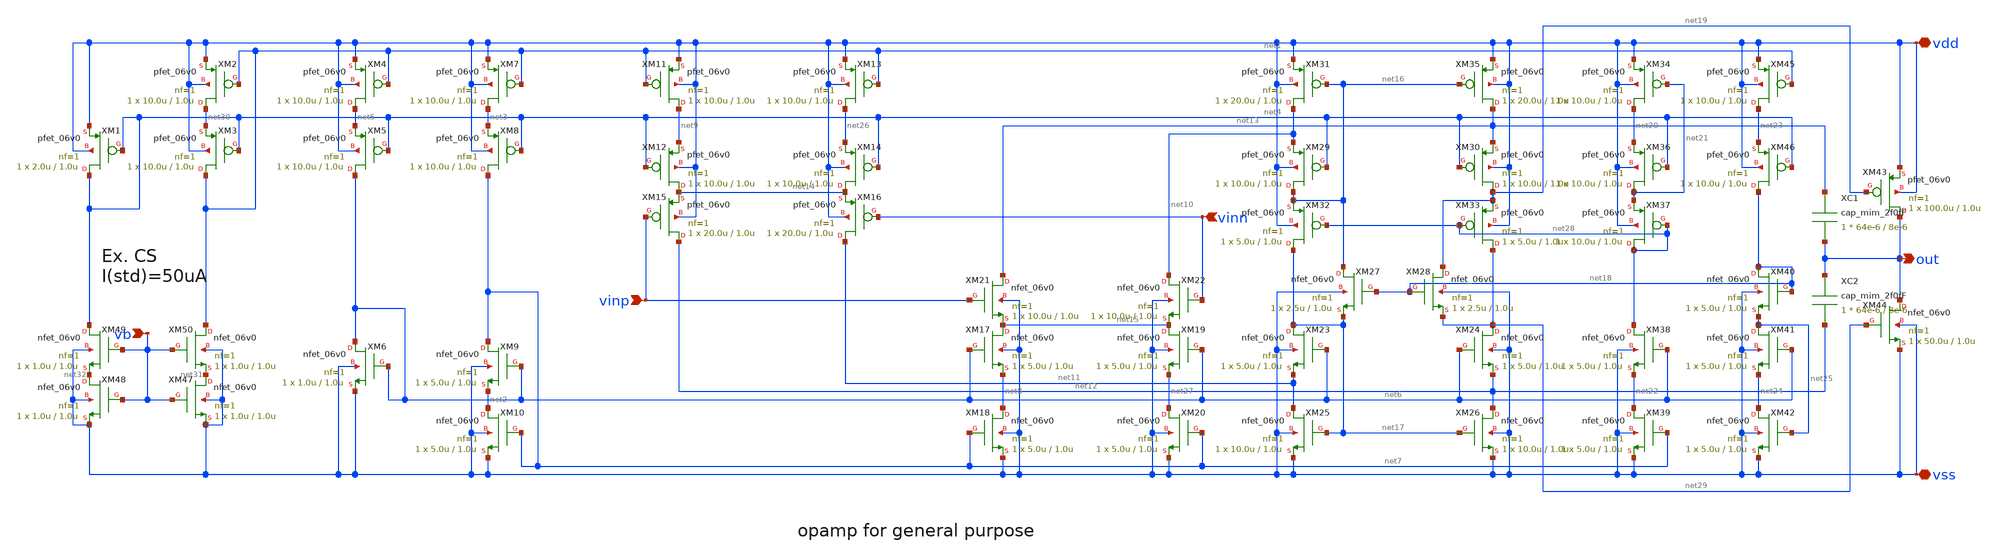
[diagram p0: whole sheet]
** sch_path: member_project/3zki/opamp.sch
**.subckt opamp out vdd vss vinp vinn vb
*.opin out
*.iopin vdd
*.iopin vss
*.ipin vinp
*.ipin vinn
*.ipin vb
XM4 net5 net1 vdd vdd pfet_06v0 L=1.0u W=10.0u nf=1 ad='int((nf+1)/2) * W/nf * 0.18u' as='int((nf+2)/2) * W/nf * 0.18u'
+ pd='2*int((nf+1)/2) * (W/nf + 0.18u)' ps='2*int((nf+2)/2) * (W/nf + 0.18u)' nrd='0.18u / W' nrs='0.18u / W'
+ sa=0 sb=0 sd=0 m=1
XM5 net6 net4 net5 vdd pfet_06v0 L=1.0u W=10.0u nf=1 ad='int((nf+1)/2) * W/nf * 0.18u' as='int((nf+2)/2) * W/nf * 0.18u'
+ pd='2*int((nf+1)/2) * (W/nf + 0.18u)' ps='2*int((nf+2)/2) * (W/nf + 0.18u)' nrd='0.18u / W' nrs='0.18u / W'
+ sa=0 sb=0 sd=0 m=1
XM6 net6 net6 vss vss nfet_06v0 L=1.0u W=1.0u nf=1 ad='int((nf+1)/2) * W/nf * 0.18u' as='int((nf+2)/2) * W/nf * 0.18u'
+ pd='2*int((nf+1)/2) * (W/nf + 0.18u)' ps='2*int((nf+2)/2) * (W/nf + 0.18u)' nrd='0.18u / W' nrs='0.18u / W'
+ sa=0 sb=0 sd=0 m=1
XM7 net3 net1 vdd vdd pfet_06v0 L=1.0u W=10.0u nf=1 ad='int((nf+1)/2) * W/nf * 0.18u' as='int((nf+2)/2) * W/nf * 0.18u'
+ pd='2*int((nf+1)/2) * (W/nf + 0.18u)' ps='2*int((nf+2)/2) * (W/nf + 0.18u)' nrd='0.18u / W' nrs='0.18u / W'
+ sa=0 sb=0 sd=0 m=1
XM8 net7 net4 net3 vdd pfet_06v0 L=1.0u W=10.0u nf=1 ad='int((nf+1)/2) * W/nf * 0.18u' as='int((nf+2)/2) * W/nf * 0.18u'
+ pd='2*int((nf+1)/2) * (W/nf + 0.18u)' ps='2*int((nf+2)/2) * (W/nf + 0.18u)' nrd='0.18u / W' nrs='0.18u / W'
+ sa=0 sb=0 sd=0 m=1
XM9 net7 net6 net2 vss nfet_06v0 L=1.0u W=5.0u nf=1 ad='int((nf+1)/2) * W/nf * 0.18u' as='int((nf+2)/2) * W/nf * 0.18u'
+ pd='2*int((nf+1)/2) * (W/nf + 0.18u)' ps='2*int((nf+2)/2) * (W/nf + 0.18u)' nrd='0.18u / W' nrs='0.18u / W'
+ sa=0 sb=0 sd=0 m=1
XM10 net2 net7 vss vss nfet_06v0 L=1.0u W=5.0u nf=1 ad='int((nf+1)/2) * W/nf * 0.18u' as='int((nf+2)/2) * W/nf * 0.18u'
+ pd='2*int((nf+1)/2) * (W/nf + 0.18u)' ps='2*int((nf+2)/2) * (W/nf + 0.18u)' nrd='0.18u / W' nrs='0.18u / W'
+ sa=0 sb=0 sd=0 m=1
XM11 net9 net1 vdd vdd pfet_06v0 L=1.0u W=10.0u nf=1 ad='int((nf+1)/2) * W/nf * 0.18u' as='int((nf+2)/2) * W/nf * 0.18u'
+ pd='2*int((nf+1)/2) * (W/nf + 0.18u)' ps='2*int((nf+2)/2) * (W/nf + 0.18u)' nrd='0.18u / W' nrs='0.18u / W'
+ sa=0 sb=0 sd=0 m=1
XM12 net14 net4 net9 vdd pfet_06v0 L=1.0u W=10.0u nf=1 ad='int((nf+1)/2) * W/nf * 0.18u' as='int((nf+2)/2) * W/nf * 0.18u'
+ pd='2*int((nf+1)/2) * (W/nf + 0.18u)' ps='2*int((nf+2)/2) * (W/nf + 0.18u)' nrd='0.18u / W' nrs='0.18u / W'
+ sa=0 sb=0 sd=0 m=1
XM13 net26 net1 vdd vdd pfet_06v0 L=1.0u W=10.0u nf=1 ad='int((nf+1)/2) * W/nf * 0.18u' as='int((nf+2)/2) * W/nf * 0.18u'
+ pd='2*int((nf+1)/2) * (W/nf + 0.18u)' ps='2*int((nf+2)/2) * (W/nf + 0.18u)' nrd='0.18u / W' nrs='0.18u / W'
+ sa=0 sb=0 sd=0 m=1
XM14 net14 net4 net26 vdd pfet_06v0 L=1.0u W=10.0u nf=1 ad='int((nf+1)/2) * W/nf * 0.18u' as='int((nf+2)/2) * W/nf * 0.18u'
+ pd='2*int((nf+1)/2) * (W/nf + 0.18u)' ps='2*int((nf+2)/2) * (W/nf + 0.18u)' nrd='0.18u / W' nrs='0.18u / W'
+ sa=0 sb=0 sd=0 m=1
XM15 net12 vinp net14 vdd pfet_06v0 L=1.0u W=20.0u nf=1 ad='int((nf+1)/2) * W/nf * 0.18u' as='int((nf+2)/2) * W/nf * 0.18u'
+ pd='2*int((nf+1)/2) * (W/nf + 0.18u)' ps='2*int((nf+2)/2) * (W/nf + 0.18u)' nrd='0.18u / W' nrs='0.18u / W'
+ sa=0 sb=0 sd=0 m=1
XM16 net11 vinn net14 vdd pfet_06v0 L=1.0u W=20.0u nf=1 ad='int((nf+1)/2) * W/nf * 0.18u' as='int((nf+2)/2) * W/nf * 0.18u'
+ pd='2*int((nf+1)/2) * (W/nf + 0.18u)' ps='2*int((nf+2)/2) * (W/nf + 0.18u)' nrd='0.18u / W' nrs='0.18u / W'
+ sa=0 sb=0 sd=0 m=1
XM17 net15 net6 net8 vss nfet_06v0 L=1.0u W=5.0u nf=1 ad='int((nf+1)/2) * W/nf * 0.18u' as='int((nf+2)/2) * W/nf * 0.18u'
+ pd='2*int((nf+1)/2) * (W/nf + 0.18u)' ps='2*int((nf+2)/2) * (W/nf + 0.18u)' nrd='0.18u / W' nrs='0.18u / W'
+ sa=0 sb=0 sd=0 m=1
XM18 net8 net7 vss vss nfet_06v0 L=1.0u W=5.0u nf=1 ad='int((nf+1)/2) * W/nf * 0.18u' as='int((nf+2)/2) * W/nf * 0.18u'
+ pd='2*int((nf+1)/2) * (W/nf + 0.18u)' ps='2*int((nf+2)/2) * (W/nf + 0.18u)' nrd='0.18u / W' nrs='0.18u / W'
+ sa=0 sb=0 sd=0 m=1
XM19 net15 net6 net27 vss nfet_06v0 L=1.0u W=5.0u nf=1 ad='int((nf+1)/2) * W/nf * 0.18u' as='int((nf+2)/2) * W/nf * 0.18u'
+ pd='2*int((nf+1)/2) * (W/nf + 0.18u)' ps='2*int((nf+2)/2) * (W/nf + 0.18u)' nrd='0.18u / W' nrs='0.18u / W'
+ sa=0 sb=0 sd=0 m=1
XM20 net27 net7 vss vss nfet_06v0 L=1.0u W=5.0u nf=1 ad='int((nf+1)/2) * W/nf * 0.18u' as='int((nf+2)/2) * W/nf * 0.18u'
+ pd='2*int((nf+1)/2) * (W/nf + 0.18u)' ps='2*int((nf+2)/2) * (W/nf + 0.18u)' nrd='0.18u / W' nrs='0.18u / W'
+ sa=0 sb=0 sd=0 m=1
XM21 net13 vinp net15 vss nfet_06v0 L=1.0u W=10.0u nf=1 ad='int((nf+1)/2) * W/nf * 0.18u' as='int((nf+2)/2) * W/nf * 0.18u'
+ pd='2*int((nf+1)/2) * (W/nf + 0.18u)' ps='2*int((nf+2)/2) * (W/nf + 0.18u)' nrd='0.18u / W' nrs='0.18u / W'
+ sa=0 sb=0 sd=0 m=1
XM22 net10 vinn net15 vss nfet_06v0 L=1.0u W=10.0u nf=1 ad='int((nf+1)/2) * W/nf * 0.18u' as='int((nf+2)/2) * W/nf * 0.18u'
+ pd='2*int((nf+1)/2) * (W/nf + 0.18u)' ps='2*int((nf+2)/2) * (W/nf + 0.18u)' nrd='0.18u / W' nrs='0.18u / W'
+ sa=0 sb=0 sd=0 m=1
XM29 net16 net4 net10 vdd pfet_06v0 L=1.0u W=10.0u nf=1 ad='int((nf+1)/2) * W/nf * 0.18u' as='int((nf+2)/2) * W/nf * 0.18u'
+ pd='2*int((nf+1)/2) * (W/nf + 0.18u)' ps='2*int((nf+2)/2) * (W/nf + 0.18u)' nrd='0.18u / W' nrs='0.18u / W'
+ sa=0 sb=0 sd=0 m=1
XM30 net19 net4 net13 vdd pfet_06v0 L=1.0u W=10.0u nf=1 ad='int((nf+1)/2) * W/nf * 0.18u' as='int((nf+2)/2) * W/nf * 0.18u'
+ pd='2*int((nf+1)/2) * (W/nf + 0.18u)' ps='2*int((nf+2)/2) * (W/nf + 0.18u)' nrd='0.18u / W' nrs='0.18u / W'
+ sa=0 sb=0 sd=0 m=1
XM31 net10 net16 vdd vdd pfet_06v0 L=1.0u W=20.0u nf=1 ad='int((nf+1)/2) * W/nf * 0.18u' as='int((nf+2)/2) * W/nf * 0.18u'
+ pd='2*int((nf+1)/2) * (W/nf + 0.18u)' ps='2*int((nf+2)/2) * (W/nf + 0.18u)' nrd='0.18u / W' nrs='0.18u / W'
+ sa=0 sb=0 sd=0 m=1
XM35 net13 net16 vdd vdd pfet_06v0 L=1.0u W=20.0u nf=1 ad='int((nf+1)/2) * W/nf * 0.18u' as='int((nf+2)/2) * W/nf * 0.18u'
+ pd='2*int((nf+1)/2) * (W/nf + 0.18u)' ps='2*int((nf+2)/2) * (W/nf + 0.18u)' nrd='0.18u / W' nrs='0.18u / W'
+ sa=0 sb=0 sd=0 m=1
XM32 net17 net28 net16 vdd pfet_06v0 L=1.0u W=5.0u nf=1 ad='int((nf+1)/2) * W/nf * 0.18u' as='int((nf+2)/2) * W/nf * 0.18u'
+ pd='2*int((nf+1)/2) * (W/nf + 0.18u)' ps='2*int((nf+2)/2) * (W/nf + 0.18u)' nrd='0.18u / W' nrs='0.18u / W'
+ sa=0 sb=0 sd=0 m=1
XM33 net29 net28 net19 vdd pfet_06v0 L=1.0u W=5.0u nf=1 ad='int((nf+1)/2) * W/nf * 0.18u' as='int((nf+2)/2) * W/nf * 0.18u'
+ pd='2*int((nf+1)/2) * (W/nf + 0.18u)' ps='2*int((nf+2)/2) * (W/nf + 0.18u)' nrd='0.18u / W' nrs='0.18u / W'
+ sa=0 sb=0 sd=0 m=1
XM23 net17 net6 net11 vss nfet_06v0 L=1.0u W=5.0u nf=1 ad='int((nf+1)/2) * W/nf * 0.18u' as='int((nf+2)/2) * W/nf * 0.18u'
+ pd='2*int((nf+1)/2) * (W/nf + 0.18u)' ps='2*int((nf+2)/2) * (W/nf + 0.18u)' nrd='0.18u / W' nrs='0.18u / W'
+ sa=0 sb=0 sd=0 m=1
XM24 net29 net6 net12 vss nfet_06v0 L=1.0u W=5.0u nf=1 ad='int((nf+1)/2) * W/nf * 0.18u' as='int((nf+2)/2) * W/nf * 0.18u'
+ pd='2*int((nf+1)/2) * (W/nf + 0.18u)' ps='2*int((nf+2)/2) * (W/nf + 0.18u)' nrd='0.18u / W' nrs='0.18u / W'
+ sa=0 sb=0 sd=0 m=1
XM25 net11 net17 vss vss nfet_06v0 L=1.0u W=10.0u nf=1 ad='int((nf+1)/2) * W/nf * 0.18u' as='int((nf+2)/2) * W/nf * 0.18u'
+ pd='2*int((nf+1)/2) * (W/nf + 0.18u)' ps='2*int((nf+2)/2) * (W/nf + 0.18u)' nrd='0.18u / W' nrs='0.18u / W'
+ sa=0 sb=0 sd=0 m=1
XM26 net12 net17 vss vss nfet_06v0 L=1.0u W=10.0u nf=1 ad='int((nf+1)/2) * W/nf * 0.18u' as='int((nf+2)/2) * W/nf * 0.18u'
+ pd='2*int((nf+1)/2) * (W/nf + 0.18u)' ps='2*int((nf+2)/2) * (W/nf + 0.18u)' nrd='0.18u / W' nrs='0.18u / W'
+ sa=0 sb=0 sd=0 m=1
XM27 net16 net18 net17 vss nfet_06v0 L=1.0u W=2.5u nf=1 ad='int((nf+1)/2) * W/nf * 0.18u' as='int((nf+2)/2) * W/nf * 0.18u'
+ pd='2*int((nf+1)/2) * (W/nf + 0.18u)' ps='2*int((nf+2)/2) * (W/nf + 0.18u)' nrd='0.18u / W' nrs='0.18u / W'
+ sa=0 sb=0 sd=0 m=1
XM28 net19 net18 net29 vss nfet_06v0 L=1.0u W=2.5u nf=1 ad='int((nf+1)/2) * W/nf * 0.18u' as='int((nf+2)/2) * W/nf * 0.18u'
+ pd='2*int((nf+1)/2) * (W/nf + 0.18u)' ps='2*int((nf+2)/2) * (W/nf + 0.18u)' nrd='0.18u / W' nrs='0.18u / W'
+ sa=0 sb=0 sd=0 m=1
XM34 net20 net21 vdd vdd pfet_06v0 L=1.0u W=10.0u nf=1 ad='int((nf+1)/2) * W/nf * 0.18u' as='int((nf+2)/2) * W/nf * 0.18u'
+ pd='2*int((nf+1)/2) * (W/nf + 0.18u)' ps='2*int((nf+2)/2) * (W/nf + 0.18u)' nrd='0.18u / W' nrs='0.18u / W'
+ sa=0 sb=0 sd=0 m=1
XM36 net21 net4 net20 vdd pfet_06v0 L=1.0u W=10.0u nf=1 ad='int((nf+1)/2) * W/nf * 0.18u' as='int((nf+2)/2) * W/nf * 0.18u'
+ pd='2*int((nf+1)/2) * (W/nf + 0.18u)' ps='2*int((nf+2)/2) * (W/nf + 0.18u)' nrd='0.18u / W' nrs='0.18u / W'
+ sa=0 sb=0 sd=0 m=1
XM37 net28 net28 net21 vdd pfet_06v0 L=1.0u W=10.0u nf=1 ad='int((nf+1)/2) * W/nf * 0.18u' as='int((nf+2)/2) * W/nf * 0.18u'
+ pd='2*int((nf+1)/2) * (W/nf + 0.18u)' ps='2*int((nf+2)/2) * (W/nf + 0.18u)' nrd='0.18u / W' nrs='0.18u / W'
+ sa=0 sb=0 sd=0 m=1
XM38 net28 net6 net22 vss nfet_06v0 L=1.0u W=5.0u nf=1 ad='int((nf+1)/2) * W/nf * 0.18u' as='int((nf+2)/2) * W/nf * 0.18u'
+ pd='2*int((nf+1)/2) * (W/nf + 0.18u)' ps='2*int((nf+2)/2) * (W/nf + 0.18u)' nrd='0.18u / W' nrs='0.18u / W'
+ sa=0 sb=0 sd=0 m=1
XM39 net22 net7 vss vss nfet_06v0 L=1.0u W=5.0u nf=1 ad='int((nf+1)/2) * W/nf * 0.18u' as='int((nf+2)/2) * W/nf * 0.18u'
+ pd='2*int((nf+1)/2) * (W/nf + 0.18u)' ps='2*int((nf+2)/2) * (W/nf + 0.18u)' nrd='0.18u / W' nrs='0.18u / W'
+ sa=0 sb=0 sd=0 m=1
XM45 net23 net1 vdd vdd pfet_06v0 L=1.0u W=10.0u nf=1 ad='int((nf+1)/2) * W/nf * 0.18u' as='int((nf+2)/2) * W/nf * 0.18u'
+ pd='2*int((nf+1)/2) * (W/nf + 0.18u)' ps='2*int((nf+2)/2) * (W/nf + 0.18u)' nrd='0.18u / W' nrs='0.18u / W'
+ sa=0 sb=0 sd=0 m=1
XM46 net18 net4 net23 vdd pfet_06v0 L=1.0u W=10.0u nf=1 ad='int((nf+1)/2) * W/nf * 0.18u' as='int((nf+2)/2) * W/nf * 0.18u'
+ pd='2*int((nf+1)/2) * (W/nf + 0.18u)' ps='2*int((nf+2)/2) * (W/nf + 0.18u)' nrd='0.18u / W' nrs='0.18u / W'
+ sa=0 sb=0 sd=0 m=1
XM40 net18 net18 net25 vss nfet_06v0 L=1.0u W=5.0u nf=1 ad='int((nf+1)/2) * W/nf * 0.18u' as='int((nf+2)/2) * W/nf * 0.18u'
+ pd='2*int((nf+1)/2) * (W/nf + 0.18u)' ps='2*int((nf+2)/2) * (W/nf + 0.18u)' nrd='0.18u / W' nrs='0.18u / W'
+ sa=0 sb=0 sd=0 m=1
XM41 net25 net6 net24 vss nfet_06v0 L=1.0u W=5.0u nf=1 ad='int((nf+1)/2) * W/nf * 0.18u' as='int((nf+2)/2) * W/nf * 0.18u'
+ pd='2*int((nf+1)/2) * (W/nf + 0.18u)' ps='2*int((nf+2)/2) * (W/nf + 0.18u)' nrd='0.18u / W' nrs='0.18u / W'
+ sa=0 sb=0 sd=0 m=1
XM42 net24 net25 vss vss nfet_06v0 L=1.0u W=5.0u nf=1 ad='int((nf+1)/2) * W/nf * 0.18u' as='int((nf+2)/2) * W/nf * 0.18u'
+ pd='2*int((nf+1)/2) * (W/nf + 0.18u)' ps='2*int((nf+2)/2) * (W/nf + 0.18u)' nrd='0.18u / W' nrs='0.18u / W'
+ sa=0 sb=0 sd=0 m=1
XM43 out net19 vdd vdd pfet_06v0 L=1.0u W=100.0u nf=1 ad='int((nf+1)/2) * W/nf * 0.18u' as='int((nf+2)/2) * W/nf * 0.18u'
+ pd='2*int((nf+1)/2) * (W/nf + 0.18u)' ps='2*int((nf+2)/2) * (W/nf + 0.18u)' nrd='0.18u / W' nrs='0.18u / W'
+ sa=0 sb=0 sd=0 m=1
XM44 out net29 vss vss nfet_06v0 L=1.0u W=50.0u nf=1 ad='int((nf+1)/2) * W/nf * 0.18u' as='int((nf+2)/2) * W/nf * 0.18u'
+ pd='2*int((nf+1)/2) * (W/nf + 0.18u)' ps='2*int((nf+2)/2) * (W/nf + 0.18u)' nrd='0.18u / W' nrs='0.18u / W'
+ sa=0 sb=0 sd=0 m=1
XM1 net4 net4 vdd vdd pfet_06v0 L=1.0u W=2.0u nf=1 ad='int((nf+1)/2) * W/nf * 0.18u' as='int((nf+2)/2) * W/nf * 0.18u'
+ pd='2*int((nf+1)/2) * (W/nf + 0.18u)' ps='2*int((nf+2)/2) * (W/nf + 0.18u)' nrd='0.18u / W' nrs='0.18u / W'
+ sa=0 sb=0 sd=0 m=1
XM2 net30 net1 vdd vdd pfet_06v0 L=1.0u W=10.0u nf=1 ad='int((nf+1)/2) * W/nf * 0.18u' as='int((nf+2)/2) * W/nf * 0.18u'
+ pd='2*int((nf+1)/2) * (W/nf + 0.18u)' ps='2*int((nf+2)/2) * (W/nf + 0.18u)' nrd='0.18u / W' nrs='0.18u / W'
+ sa=0 sb=0 sd=0 m=1
XM3 net1 net4 net30 vdd pfet_06v0 L=1.0u W=10.0u nf=1 ad='int((nf+1)/2) * W/nf * 0.18u' as='int((nf+2)/2) * W/nf * 0.18u'
+ pd='2*int((nf+1)/2) * (W/nf + 0.18u)' ps='2*int((nf+2)/2) * (W/nf + 0.18u)' nrd='0.18u / W' nrs='0.18u / W'
+ sa=0 sb=0 sd=0 m=1
XM47 net31 vb vss vss nfet_06v0 L=1.0u W=1.0u nf=1 ad='int((nf+1)/2) * W/nf * 0.18u' as='int((nf+2)/2) * W/nf * 0.18u'
+ pd='2*int((nf+1)/2) * (W/nf + 0.18u)' ps='2*int((nf+2)/2) * (W/nf + 0.18u)' nrd='0.18u / W' nrs='0.18u / W'
+ sa=0 sb=0 sd=0 m=1
XM48 net32 vb vss vss nfet_06v0 L=1.0u W=1.0u nf=1 ad='int((nf+1)/2) * W/nf * 0.18u' as='int((nf+2)/2) * W/nf * 0.18u'
+ pd='2*int((nf+1)/2) * (W/nf + 0.18u)' ps='2*int((nf+2)/2) * (W/nf + 0.18u)' nrd='0.18u / W' nrs='0.18u / W'
+ sa=0 sb=0 sd=0 m=1
XM49 net4 vb net32 vss nfet_06v0 L=1.0u W=1.0u nf=1 ad='int((nf+1)/2) * W/nf * 0.18u' as='int((nf+2)/2) * W/nf * 0.18u'
+ pd='2*int((nf+1)/2) * (W/nf + 0.18u)' ps='2*int((nf+2)/2) * (W/nf + 0.18u)' nrd='0.18u / W' nrs='0.18u / W'
+ sa=0 sb=0 sd=0 m=1
XM50 net1 vb net31 vss nfet_06v0 L=1.0u W=1.0u nf=1 ad='int((nf+1)/2) * W/nf * 0.18u' as='int((nf+2)/2) * W/nf * 0.18u'
+ pd='2*int((nf+1)/2) * (W/nf + 0.18u)' ps='2*int((nf+2)/2) * (W/nf + 0.18u)' nrd='0.18u / W' nrs='0.18u / W'
+ sa=0 sb=0 sd=0 m=1
XC1 net13 out cap_mim_2f0fF c_width=64e-6 c_length=8e-6 m=1
XC2 out net12 cap_mim_2f0fF c_width=64e-6 c_length=8e-6 m=1
**.ends
.end
